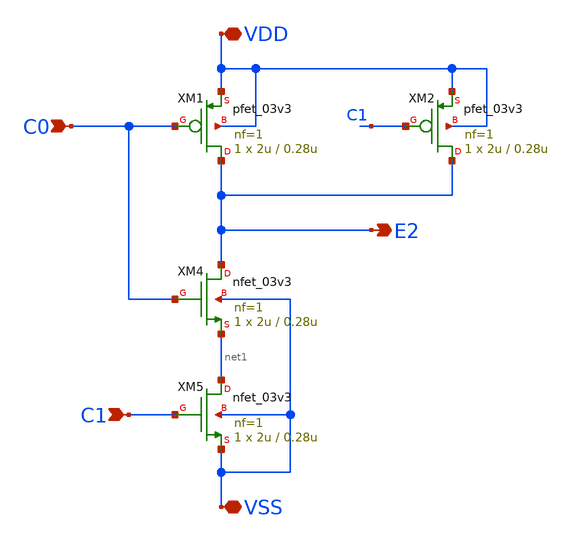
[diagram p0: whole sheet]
** sch_path: designs/digital/schematic/nand.sch
**.subckt nand VDD VSS C0 E2 C1
*.iopin VDD
*.iopin VSS
*.ipin C0
*.opin E2
*.ipin C1
XM1 E2 C0 VDD VDD pfet_03v3 L=0.28u W=2u nf=1 ad='int((nf+1)/2) * W/nf * 0.18u' as='int((nf+2)/2) * W/nf * 0.18u'
+ pd='2*int((nf+1)/2) * (W/nf + 0.18u)' ps='2*int((nf+2)/2) * (W/nf + 0.18u)' nrd='0.18u / W' nrs='0.18u / W'
+ sa=0 sb=0 sd=0 m=1
XM2 E2 C1 VDD VDD pfet_03v3 L=0.28u W=2u nf=1 ad='int((nf+1)/2) * W/nf * 0.18u' as='int((nf+2)/2) * W/nf * 0.18u'
+ pd='2*int((nf+1)/2) * (W/nf + 0.18u)' ps='2*int((nf+2)/2) * (W/nf + 0.18u)' nrd='0.18u / W' nrs='0.18u / W'
+ sa=0 sb=0 sd=0 m=1
XM4 E2 C0 net1 VSS nfet_03v3 L=0.28u W=2u nf=1 ad='int((nf+1)/2) * W/nf * 0.18u' as='int((nf+2)/2) * W/nf * 0.18u'
+ pd='2*int((nf+1)/2) * (W/nf + 0.18u)' ps='2*int((nf+2)/2) * (W/nf + 0.18u)' nrd='0.18u / W' nrs='0.18u / W'
+ sa=0 sb=0 sd=0 m=1
XM5 net1 C1 VSS VSS nfet_03v3 L=0.28u W=2u nf=1 ad='int((nf+1)/2) * W/nf * 0.18u' as='int((nf+2)/2) * W/nf * 0.18u'
+ pd='2*int((nf+1)/2) * (W/nf + 0.18u)' ps='2*int((nf+2)/2) * (W/nf + 0.18u)' nrd='0.18u / W' nrs='0.18u / W'
+ sa=0 sb=0 sd=0 m=1
**.ends
.end
